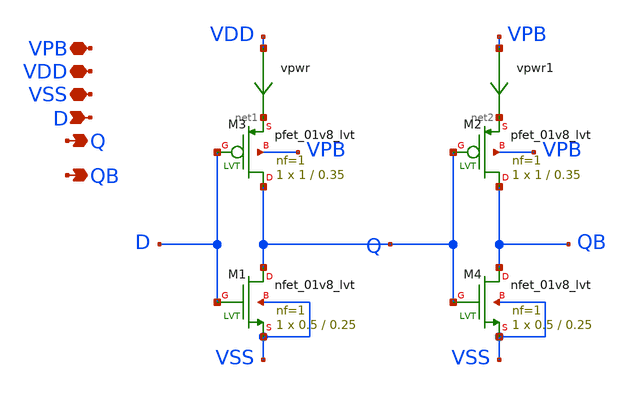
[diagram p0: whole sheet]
** sch_path: xschem/pll_inv1_buf.sch
**.subckt pll_inv1_buf Q D VDD VPB VSS QB
*.opin Q
*.ipin D
*.iopin VDD
*.iopin VPB
*.iopin VSS
*.opin QB
XM3 Q D net1 VPB sky130_fd_pr__pfet_01v8_lvt L=0.35 W=1 nf=1 ad='int((nf+1)/2) * W/nf * 0.29' as='int((nf+2)/2) * W/nf * 0.29'
+ pd='2*int((nf+1)/2) * (W/nf + 0.29)' ps='2*int((nf+2)/2) * (W/nf + 0.29)' nrd='0.29 / W' nrs='0.29 / W'
+ sa=0 sb=0 sd=0 mult=1 m=1
vpwr VDD net1 0
.save i(vpwr)
XM1 Q D VSS VSS sky130_fd_pr__nfet_01v8_lvt L=0.25 W=0.5 nf=1 ad='int((nf+1)/2) * W/nf * 0.29' as='int((nf+2)/2) * W/nf * 0.29'
+ pd='2*int((nf+1)/2) * (W/nf + 0.29)' ps='2*int((nf+2)/2) * (W/nf + 0.29)' nrd='0.29 / W' nrs='0.29 / W'
+ sa=0 sb=0 sd=0 mult=1 m=1
XM2 QB Q net2 VPB sky130_fd_pr__pfet_01v8_lvt L=0.35 W=1 nf=1 ad='int((nf+1)/2) * W/nf * 0.29' as='int((nf+2)/2) * W/nf * 0.29'
+ pd='2*int((nf+1)/2) * (W/nf + 0.29)' ps='2*int((nf+2)/2) * (W/nf + 0.29)' nrd='0.29 / W' nrs='0.29 / W'
+ sa=0 sb=0 sd=0 mult=1 m=1
vpwr1 VPB net2 0
.save i(vpwr1)
XM4 QB Q VSS VSS sky130_fd_pr__nfet_01v8_lvt L=0.25 W=0.5 nf=1 ad='int((nf+1)/2) * W/nf * 0.29' as='int((nf+2)/2) * W/nf * 0.29'
+ pd='2*int((nf+1)/2) * (W/nf + 0.29)' ps='2*int((nf+2)/2) * (W/nf + 0.29)' nrd='0.29 / W' nrs='0.29 / W'
+ sa=0 sb=0 sd=0 mult=1 m=1
**.ends
.end
